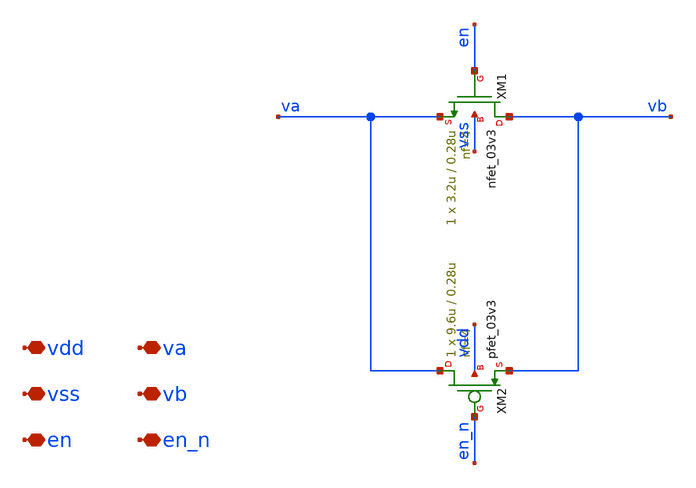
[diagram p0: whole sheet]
** sch_path: xschem/sw/b9_sw_debug.sch
**.subckt b9_sw_debug vdd vss en va vb en_n
*.iopin vdd
*.iopin vss
*.iopin en
*.iopin va
*.iopin vb
*.iopin en_n
XM1 vb en va vss nfet_03v3 L=0.28u W=3.2u nf=4 ad='int((nf+1)/2) * W/nf * 0.18u' as='int((nf+2)/2) * W/nf * 0.18u'
+ pd='2*int((nf+1)/2) * (W/nf + 0.18u)' ps='2*int((nf+2)/2) * (W/nf + 0.18u)' nrd='0.18u / W' nrs='0.18u / W'
+ sa=0 sb=0 sd=0 m=1
XM2 va en_n vb vdd pfet_03v3 L=0.28u W=9.6u nf=4 ad='int((nf+1)/2) * W/nf * 0.18u' as='int((nf+2)/2) * W/nf * 0.18u'
+ pd='2*int((nf+1)/2) * (W/nf + 0.18u)' ps='2*int((nf+2)/2) * (W/nf + 0.18u)' nrd='0.18u / W' nrs='0.18u / W'
+ sa=0 sb=0 sd=0 m=1
**.ends
.end
